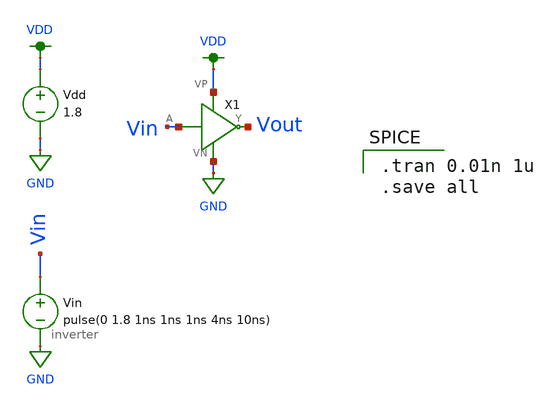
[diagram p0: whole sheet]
** sch_path: 1_And_Gate/inverter_test.sch
**.subckt inverter_test
X1 Vin Vout VDD GND inverter
Vdd VDD GND 1.8
Vin Vin GND pulse(0 1.8 1ns 1ns 1ns 4ns 10ns)
**** begin user architecture code

.tran 0.01n 1u
.save all


.option wnflag=1
.lib ~/skywater/skywater-pdk/libraries/sky130_fd_pr_ngspice/latest/models/sky130.lib.spice tt

**** end user architecture code
**.ends

* expanding   symbol:
*+  /home/pranaviboyalakuntla/Documents/Mixed-Analog-Digital-VLSI/1_And_Gate/inverter.sym # of pins=4
** sym_path: 1_And_Gate/inverter.sym
** sch_path: 1_And_Gate/inverter.sch
.subckt inverter A Y VP VN
*.ipin A
*.iopin VP
*.iopin VN
*.opin Y
XM1 Y A VP VDD sky130_fd_pr__pfet_01v8 L=0.15 W=1 nf=1 ad='int((nf+1)/2) * W/nf * 0.29' as='int((nf+2)/2) * W/nf * 0.29'
+ pd='2*int((nf+1)/2) * (W/nf + 0.29)' ps='2*int((nf+2)/2) * (W/nf + 0.29)' nrd='0.29 / W' nrs='0.29 / W'
+ sa=0 sb=0 sd=0 mult=1 m=1
XM2 Y A VN GND sky130_fd_pr__nfet_01v8 L=0.15 W=1 nf=1 ad='int((nf+1)/2) * W/nf * 0.29' as='int((nf+2)/2) * W/nf * 0.29'
+ pd='2*int((nf+1)/2) * (W/nf + 0.29)' ps='2*int((nf+2)/2) * (W/nf + 0.29)' nrd='0.29 / W' nrs='0.29 / W'
+ sa=0 sb=0 sd=0 mult=1 m=1
.ends

.GLOBAL VDD
.GLOBAL GND
.end
